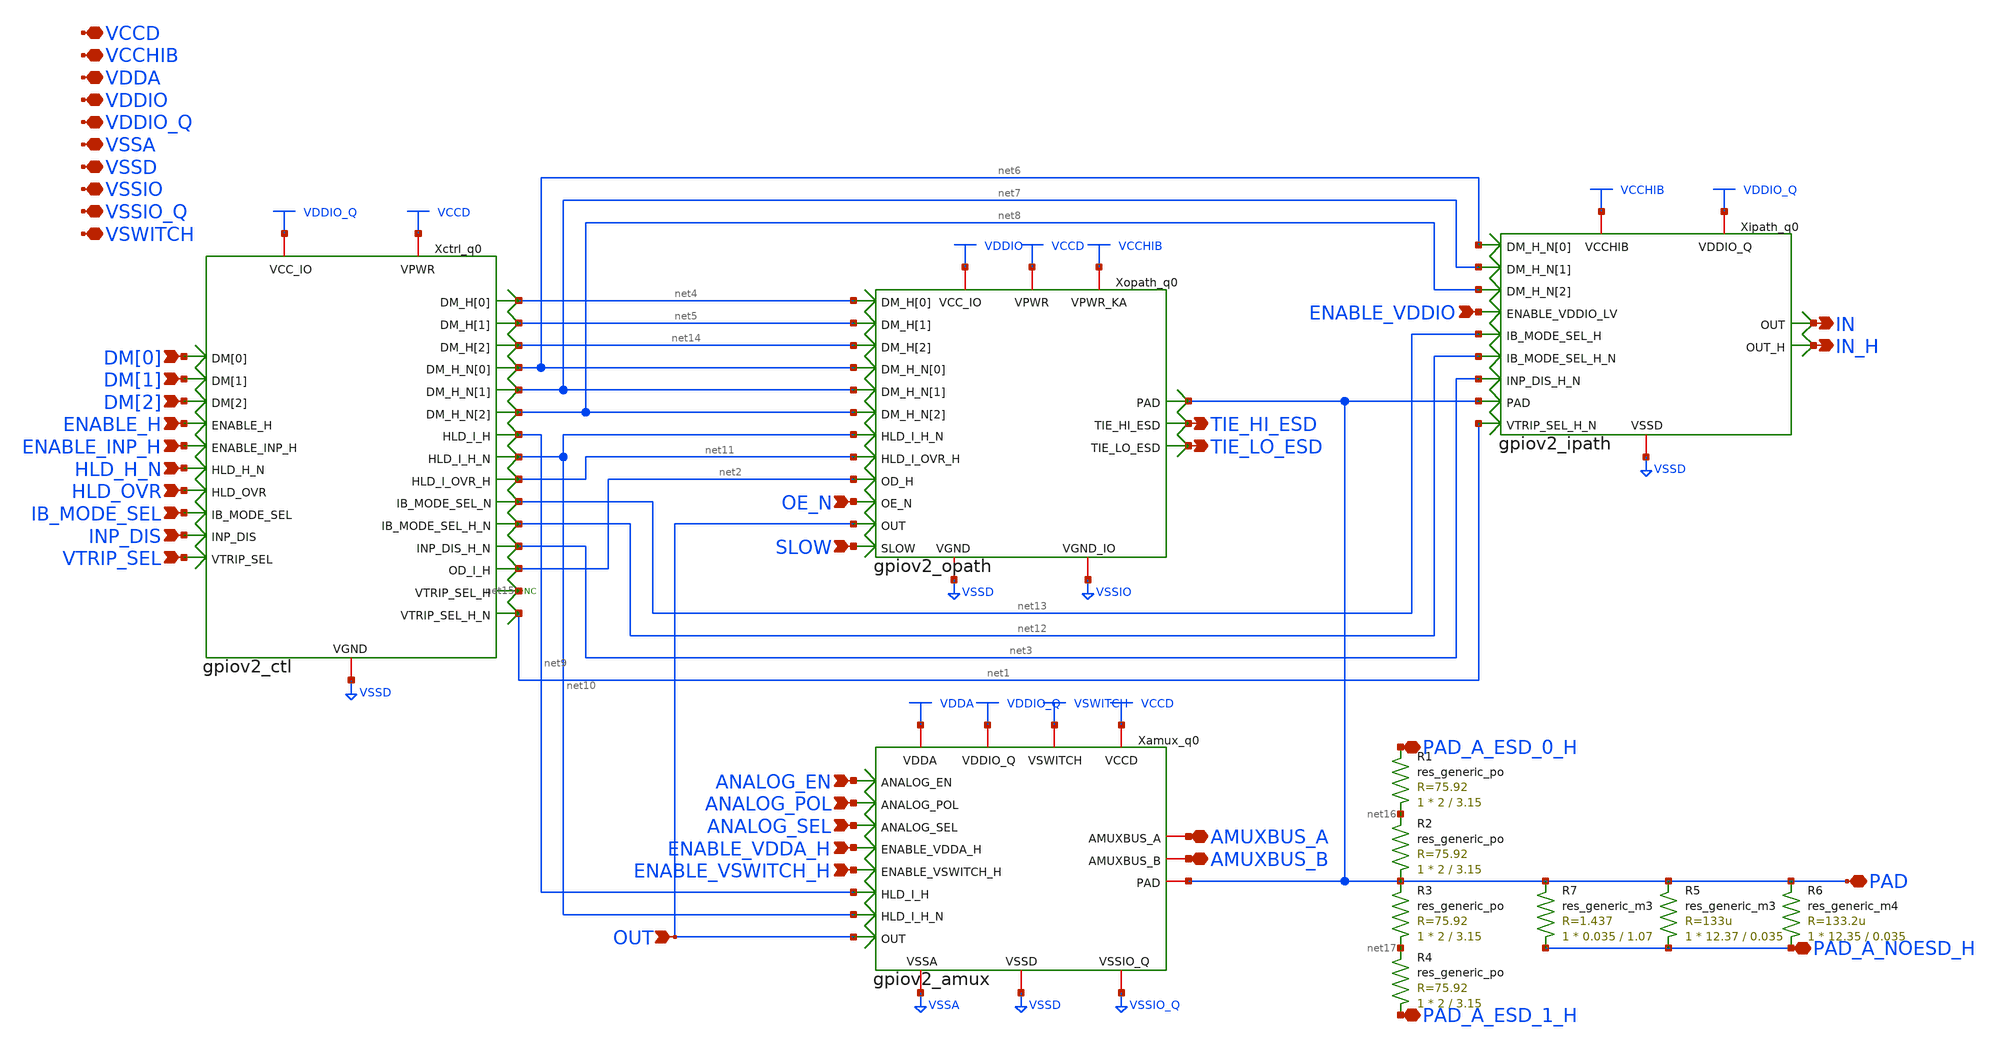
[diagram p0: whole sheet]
** sch_path: top_gpiov2.sch
* Copyright 2023 David Mitchell Bailey
* Licensed under the Apache License, Version 2.0 (the "License");
* you may not use this file except in compliance with the License.
* You may obtain a copy of the License at
* https://www.apache.org/licenses/LICENSE-2.0
* Unless required by applicable law or agreed to in writing, software
* distributed under the License is distributed on an "AS IS" BASIS,
* WITHOUT WARRANTIES OR CONDITIONS OF ANY KIND, either express or implied.
* See the License for the specific language governing permissions and
* limitations under the License.
**.subckt top_gpiov2 DM[0] VDDIO TIE_HI_ESD TIE_LO_ESD DM[1] DM[2] ENABLE_H ENABLE_INP_H HLD_H_N
*+ HLD_OVR IB_MODE_SEL INP_DIS VTRIP_SEL VDDIO_Q VSSA VSSD VSSIO ANALOG_EN ANALOG_POL ANALOG_SEL AMUXBUS_A
*+ AMUXBUS_B VCCD VCCHIB VDDA VSSIO_Q VSWITCH PAD ENABLE_VDDA_H ENABLE_VSWITCH_H IN IN_H OE_N SLOW OUT
*+ ENABLE_VDDIO PAD_A_ESD_0_H PAD_A_ESD_1_H PAD_A_NOESD_H
*.ipin DM[0]
*.iopin VDDIO
*.opin TIE_HI_ESD
*.opin TIE_LO_ESD
*.ipin DM[1]
*.ipin DM[2]
*.ipin ENABLE_H
*.ipin ENABLE_INP_H
*.ipin HLD_H_N
*.ipin HLD_OVR
*.ipin IB_MODE_SEL
*.ipin INP_DIS
*.ipin VTRIP_SEL
*.iopin VDDIO_Q
*.iopin VSSA
*.iopin VSSD
*.iopin VSSIO
*.ipin ANALOG_EN
*.ipin ANALOG_POL
*.ipin ANALOG_SEL
*.iopin AMUXBUS_A
*.iopin AMUXBUS_B
*.iopin VCCD
*.iopin VCCHIB
*.iopin VDDA
*.iopin VSSIO_Q
*.iopin VSWITCH
*.iopin PAD
*.ipin ENABLE_VDDA_H
*.ipin ENABLE_VSWITCH_H
*.opin IN
*.opin IN_H
*.ipin OE_N
*.ipin SLOW
*.ipin OUT
*.ipin ENABLE_VDDIO
*.iopin PAD_A_ESD_0_H
*.iopin PAD_A_ESD_1_H
*.iopin PAD_A_NOESD_H
* noconn #net15
Xctrl_q0 VDDIO_Q VCCD VSSD net4 net5 DM[0] net14 DM[1] DM[2] net6 net10 net9 ENABLE_H net7 HLD_H_N
+ IB_MODE_SEL net8 net11 HLD_OVR INP_DIS net13 net12 net3 VTRIP_SEL net15 net1 net2 ENABLE_INP_H gpiov2_ctl
Xamux_q0 VDDA VDDIO_Q VSWITCH VCCD VSSA VSSD VSSIO_Q AMUXBUS_A ANALOG_EN ANALOG_POL ANALOG_SEL
+ ENABLE_VDDA_H PAD ENABLE_VSWITCH_H net9 net10 OUT AMUXBUS_B gpiov2_amux
Xopath_q0 VDDIO VCCD VCCHIB VSSD VSSIO net4 net5 net14 net6 net7 PAD net8 TIE_HI_ESD net10
+ TIE_LO_ESD net11 net2 OE_N OUT SLOW gpiov2_opath
Xipath_q0 VCCHIB VDDIO_Q VSSD ENABLE_VDDIO net6 net7 net8 net13 PAD net12 net3 net1 IN IN_H
+ gpiov2_ipath
XR1 net16 PAD_A_ESD_0_H sky130_fd_pr__res_generic_po W=2 L=3.15 m=1
XR2 PAD net16 sky130_fd_pr__res_generic_po W=2 L=3.15 m=1
XR3 net17 PAD sky130_fd_pr__res_generic_po W=2 L=3.15 m=1
XR4 PAD_A_ESD_1_H net17 sky130_fd_pr__res_generic_po W=2 L=3.15 m=1
R5 PAD_A_NOESD_H PAD sky130_fd_pr__res_generic_m3 W=12.37 L=0.035 m=1
R6 PAD_A_NOESD_H PAD sky130_fd_pr__res_generic_m4 W=12.35 L=0.035 m=1
R7 PAD_A_NOESD_H PAD sky130_fd_pr__res_generic_m3 W=0.035 L=1.07 m=1
**.ends
.end
